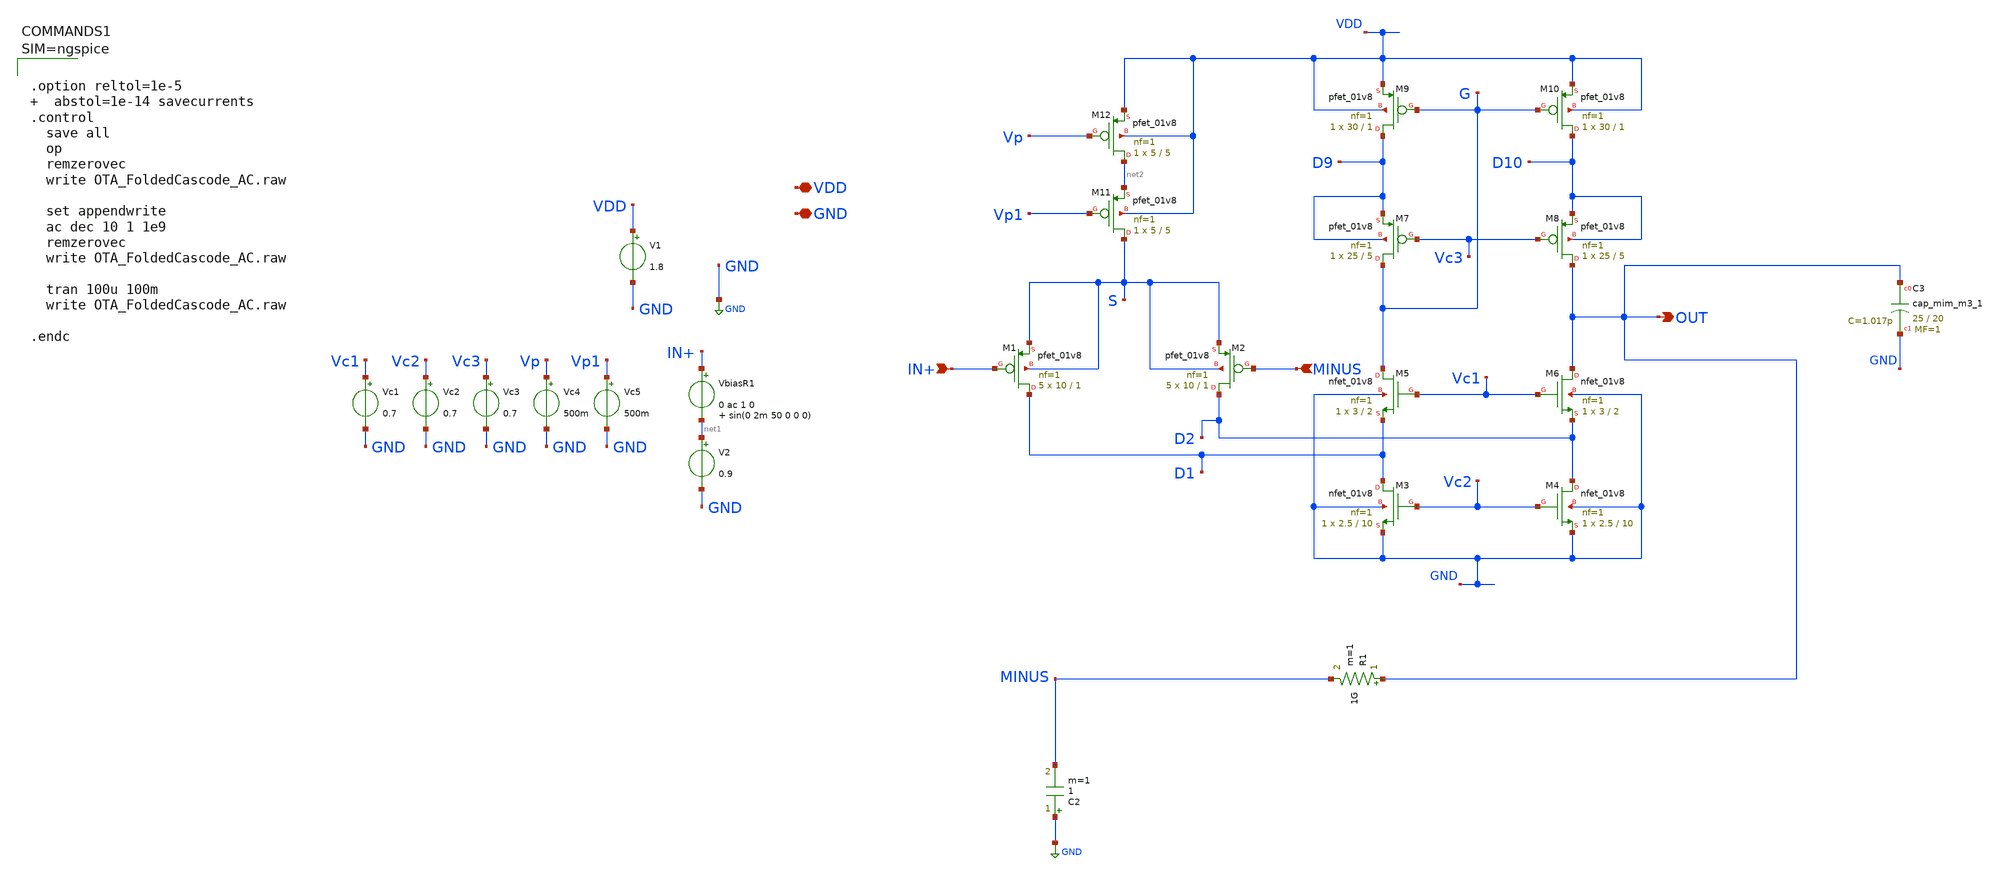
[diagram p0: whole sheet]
** sch_path: xschem/OTA_FoldedCascode_AC.sch
**.subckt OTA_FoldedCascode_AC VDD GND IN+ MINUS OUT
*.iopin VDD
*.iopin GND
*.ipin IN+
*.ipin MINUS
*.opin OUT
VbiasR1 IN+ net1 0 ac 1 0 sin(0 2m 50 0 0 0)
V2 net1 GND 0.9
XC3 OUT GND sky130_fd_pr__cap_mim_m3_1 W=25 L=20 MF=1 m=1
C2 GND MINUS 1 m=1
R1 OUT MINUS 1G m=1
V1 VDD GND 1.8
XM1 D1 IN+ S S sky130_fd_pr__pfet_01v8 L=1 W=10 nf=1 ad='int((nf+1)/2) * W/nf * 0.29' as='int((nf+2)/2) * W/nf * 0.29'
+ pd='2*int((nf+1)/2) * (W/nf + 0.29)' ps='2*int((nf+2)/2) * (W/nf + 0.29)' nrd='0.29 / W' nrs='0.29 / W'
+ sa=0 sb=0 sd=0 mult=5 m=5
XM2 D2 MINUS S S sky130_fd_pr__pfet_01v8 L=1 W=10 nf=1 ad='int((nf+1)/2) * W/nf * 0.29' as='int((nf+2)/2) * W/nf * 0.29'
+ pd='2*int((nf+1)/2) * (W/nf + 0.29)' ps='2*int((nf+2)/2) * (W/nf + 0.29)' nrd='0.29 / W' nrs='0.29 / W'
+ sa=0 sb=0 sd=0 mult=5 m=5
XM3 D1 Vc2 GND GND sky130_fd_pr__nfet_01v8 L=10 W=2.5 nf=1 ad='int((nf+1)/2) * W/nf * 0.29' as='int((nf+2)/2) * W/nf * 0.29'
+ pd='2*int((nf+1)/2) * (W/nf + 0.29)' ps='2*int((nf+2)/2) * (W/nf + 0.29)' nrd='0.29 / W' nrs='0.29 / W'
+ sa=0 sb=0 sd=0 mult=1 m=1
XM4 D2 Vc2 GND GND sky130_fd_pr__nfet_01v8 L=10 W=2.5 nf=1 ad='int((nf+1)/2) * W/nf * 0.29' as='int((nf+2)/2) * W/nf * 0.29'
+ pd='2*int((nf+1)/2) * (W/nf + 0.29)' ps='2*int((nf+2)/2) * (W/nf + 0.29)' nrd='0.29 / W' nrs='0.29 / W'
+ sa=0 sb=0 sd=0 mult=1 m=1
XM5 G Vc1 D1 GND sky130_fd_pr__nfet_01v8 L=2 W=3 nf=1 ad='int((nf+1)/2) * W/nf * 0.29' as='int((nf+2)/2) * W/nf * 0.29'
+ pd='2*int((nf+1)/2) * (W/nf + 0.29)' ps='2*int((nf+2)/2) * (W/nf + 0.29)' nrd='0.29 / W' nrs='0.29 / W'
+ sa=0 sb=0 sd=0 mult=1 m=1
XM6 OUT Vc1 D2 GND sky130_fd_pr__nfet_01v8 L=2 W=3 nf=1 ad='int((nf+1)/2) * W/nf * 0.29' as='int((nf+2)/2) * W/nf * 0.29'
+ pd='2*int((nf+1)/2) * (W/nf + 0.29)' ps='2*int((nf+2)/2) * (W/nf + 0.29)' nrd='0.29 / W' nrs='0.29 / W'
+ sa=0 sb=0 sd=0 mult=1 m=1
XM7 G Vc3 D9 D9 sky130_fd_pr__pfet_01v8 L=5 W=25 nf=1 ad='int((nf+1)/2) * W/nf * 0.29' as='int((nf+2)/2) * W/nf * 0.29'
+ pd='2*int((nf+1)/2) * (W/nf + 0.29)' ps='2*int((nf+2)/2) * (W/nf + 0.29)' nrd='0.29 / W' nrs='0.29 / W'
+ sa=0 sb=0 sd=0 mult=1 m=1
XM8 OUT Vc3 D10 D10 sky130_fd_pr__pfet_01v8 L=5 W=25 nf=1 ad='int((nf+1)/2) * W/nf * 0.29' as='int((nf+2)/2) * W/nf * 0.29'
+ pd='2*int((nf+1)/2) * (W/nf + 0.29)' ps='2*int((nf+2)/2) * (W/nf + 0.29)' nrd='0.29 / W' nrs='0.29 / W'
+ sa=0 sb=0 sd=0 mult=1 m=1
XM9 D9 G VDD VDD sky130_fd_pr__pfet_01v8 L=1 W=30 nf=1 ad='int((nf+1)/2) * W/nf * 0.29' as='int((nf+2)/2) * W/nf * 0.29'
+ pd='2*int((nf+1)/2) * (W/nf + 0.29)' ps='2*int((nf+2)/2) * (W/nf + 0.29)' nrd='0.29 / W' nrs='0.29 / W'
+ sa=0 sb=0 sd=0 mult=1 m=1
XM10 D10 G VDD VDD sky130_fd_pr__pfet_01v8 L=1 W=30 nf=1 ad='int((nf+1)/2) * W/nf * 0.29' as='int((nf+2)/2) * W/nf * 0.29'
+ pd='2*int((nf+1)/2) * (W/nf + 0.29)' ps='2*int((nf+2)/2) * (W/nf + 0.29)' nrd='0.29 / W' nrs='0.29 / W'
+ sa=0 sb=0 sd=0 mult=1 m=1
Vc1 Vc1 GND 0.7
Vc2 Vc2 GND 0.7
Vc3 Vc3 GND 0.7
Vc4 Vp GND 500m
XM11 S Vp1 net2 VDD sky130_fd_pr__pfet_01v8 L=5 W=5 nf=1 ad='int((nf+1)/2) * W/nf * 0.29' as='int((nf+2)/2) * W/nf * 0.29'
+ pd='2*int((nf+1)/2) * (W/nf + 0.29)' ps='2*int((nf+2)/2) * (W/nf + 0.29)' nrd='0.29 / W' nrs='0.29 / W'
+ sa=0 sb=0 sd=0 mult=1 m=1
XM12 net2 Vp VDD VDD sky130_fd_pr__pfet_01v8 L=5 W=5 nf=1 ad='int((nf+1)/2) * W/nf * 0.29' as='int((nf+2)/2) * W/nf * 0.29'
+ pd='2*int((nf+1)/2) * (W/nf + 0.29)' ps='2*int((nf+2)/2) * (W/nf + 0.29)' nrd='0.29 / W' nrs='0.29 / W'
+ sa=0 sb=0 sd=0 mult=1 m=1
Vc5 Vp1 GND 500m
**** begin user architecture code



.option reltol=1e-5   abstol=1e-14 savecurrents
.control
  save all
  op
  remzerovec
  write OTA_FoldedCascode_AC.raw

  set appendwrite
  ac dec 10 1 1e9
  remzerovec
  write OTA_FoldedCascode_AC.raw

  tran 100u 100m
  write OTA_FoldedCascode_AC.raw

.endc



.lib $::SKYWATER_MODELS/sky130.lib.spice tt
**** end user architecture code
**.ends
.GLOBAL GND
.end
